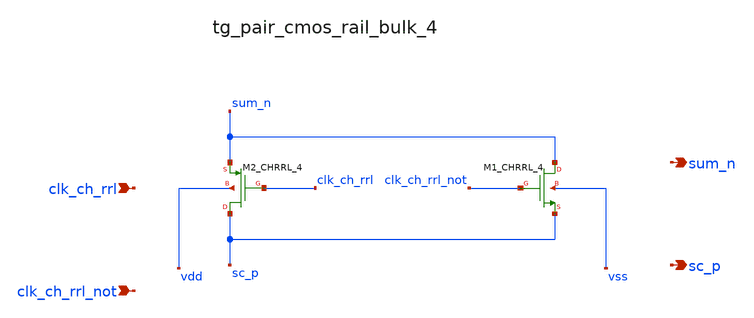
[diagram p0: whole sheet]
** sch_path: analog-db/raw/sup_003_rrl_sc_integrator/hier/blocks/tg_pair_cmos_rail_bulk_4.sch
**.subckt tg_pair_cmos_rail_bulk_4 clk_ch_rrl clk_ch_rrl_not sum_n sc_p
*.ipin clk_ch_rrl
*.ipin clk_ch_rrl_not
*.opin sum_n
*.opin sc_p
XM1_CHRRL_4 sum_n clk_ch_rrl_not sc_p vss sg13_lv_nmos w=x_dut_xm1_chrrl_4_w l=x_dut_xm1_chrrl_4_l
+ ng=1 m=x_dut_xm1_chrrl_4_m
XM2_CHRRL_4 sc_p clk_ch_rrl sum_n vdd sg13_lv_pmos w=x_dut_xm2_chrrl_4_w l=x_dut_xm2_chrrl_4_l ng=1
+ m=x_dut_xm2_chrrl_4_m
**.ends
.end
